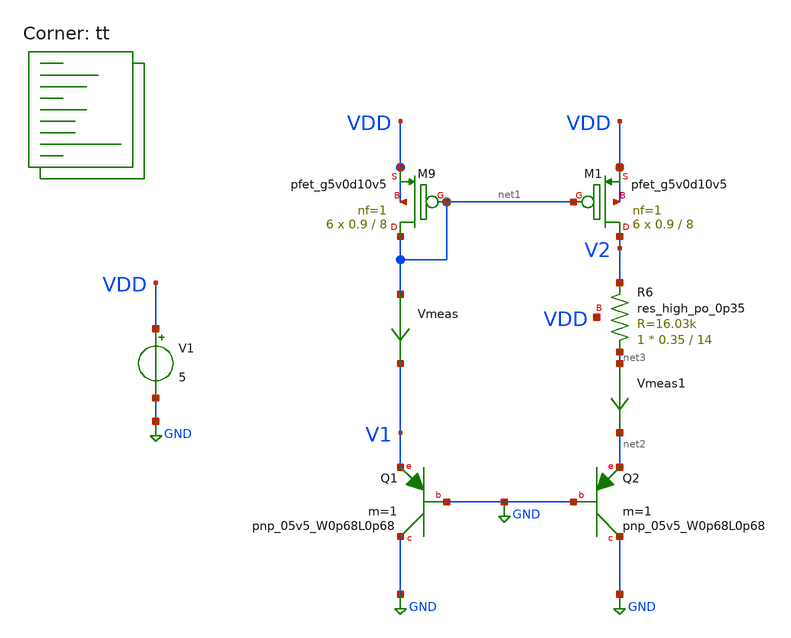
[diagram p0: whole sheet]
** sch_path: my_projects/V_REF/basic_PTAT/basic_PTAT.sch
**.subckt basic_PTAT
V1 VDD GND 5
XQ1 GND GND V1 sky130_fd_pr__pnp_05v5_W0p68L0p68 m=1
XM9 net1 net1 VDD VDD sky130_fd_pr__pfet_g5v0d10v5 L=8 W=0.9 nf=1 ad='int((1 + 1)/2) * 0.9 / 1 * 0.29'
+ as='int((1 + 2)/2) * 0.9 / 1 * 0.29' pd='2*int((1 + 1)/2) * (0.9 / 1 + 0.29)' ps='2*int((1 + 2)/2) * (0.9 / 1 + 0.29)'
+ nrd='0.29 / 0.9 ' nrs='0.29 / 0.9 ' sa=0 sb=0 sd=0 mult=6 m=6
Vmeas net1 V1 0
.save i(vmeas)
XM1 V2 net1 VDD VDD sky130_fd_pr__pfet_g5v0d10v5 L=8 W=0.9 nf=1 ad='int((1 + 1)/2) * 0.9 / 1 * 0.29'
+ as='int((1 + 2)/2) * 0.9 / 1 * 0.29' pd='2*int((1 + 1)/2) * (0.9 / 1 + 0.29)' ps='2*int((1 + 2)/2) * (0.9 / 1 + 0.29)'
+ nrd='0.29 / 0.9 ' nrs='0.29 / 0.9 ' sa=0 sb=0 sd=0 mult=6 m=6
XQ2 GND GND net2 sky130_fd_pr__pnp_05v5_W0p68L0p68 m=1
Vmeas1 net3 net2 0
.save i(vmeas1)
XR6 net3 V2 VDD sky130_fd_pr__res_high_po_0p35 L=14 mult=1 m=1
**** begin user architecture code
.lib $::SKYWATER_MODELS/sky130.lib.spice tt

**************************************************************
**************************************************************
**************************************************************
**************************************************************
**************************************************************
*LIBs*********************************************************
**************************************************************
**************************************************************
**************************************************************
**************************************************************
**************************************************************
*.lib $::SKYWATER_MODELS/sky130.lib.spice tt
* chose the corners in the corner file
* tt_mm for mismatch
* ss ff sf fs standart corners
* ll hh lh hl capacitor and resistors corners
* mc for total process variation including corners
**************************************************************
**************************************************************
**************************************************************
**************************************************************
**************************************************************
*Corners/montecarlo options***********************************
**************************************************************
**************************************************************
**************************************************************
**************************************************************
**************************************************************
.TEMP 27
**************************************************************
**************************************************************
**************************************************************
**************************************************************
*SIMULATION and Plots*****************************************
**************************************************************
**************************************************************
**************************************************************
**************************************************************
.control
save all
dc TEMP -40 125 1
*dc simulation
plot (V(V2)-V(V1))
plot deriv(V(V2)-V(V1))
plot i(Vmeas) i(Vmeas1)
.endc

**** end user architecture code
**.ends
.GLOBAL GND
.end
